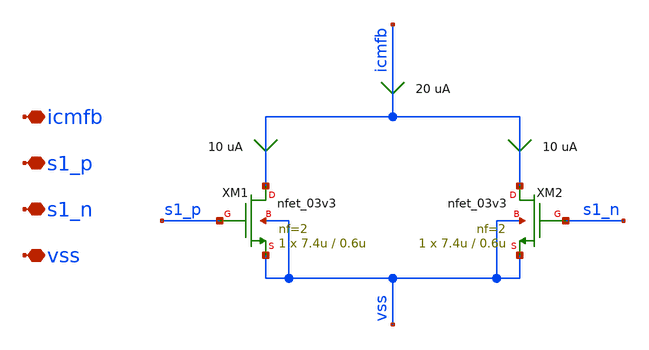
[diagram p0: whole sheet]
** sch_path: xschem/archive/ota/s1_cmfb.sch
**.subckt s1_cmfb icmfb s1_p s1_n vss
*.iopin icmfb
*.iopin s1_p
*.iopin s1_n
*.iopin vss
XM1 icmfb s1_p vss vss nfet_03v3 L=0.6u W=7.4u nf=2 ad='int((nf+1)/2) * W/nf * 0.18u' as='int((nf+2)/2) * W/nf * 0.18u'
+ pd='2*int((nf+1)/2) * (W/nf + 0.18u)' ps='2*int((nf+2)/2) * (W/nf + 0.18u)' nrd='0.18u / W' nrs='0.18u / W'
+ sa=0 sb=0 sd=0 m=1
XM2 icmfb s1_n vss vss nfet_03v3 L=0.6u W=7.4u nf=2 ad='int((nf+1)/2) * W/nf * 0.18u' as='int((nf+2)/2) * W/nf * 0.18u'
+ pd='2*int((nf+1)/2) * (W/nf + 0.18u)' ps='2*int((nf+2)/2) * (W/nf + 0.18u)' nrd='0.18u / W' nrs='0.18u / W'
+ sa=0 sb=0 sd=0 m=1
**.ends
.end
